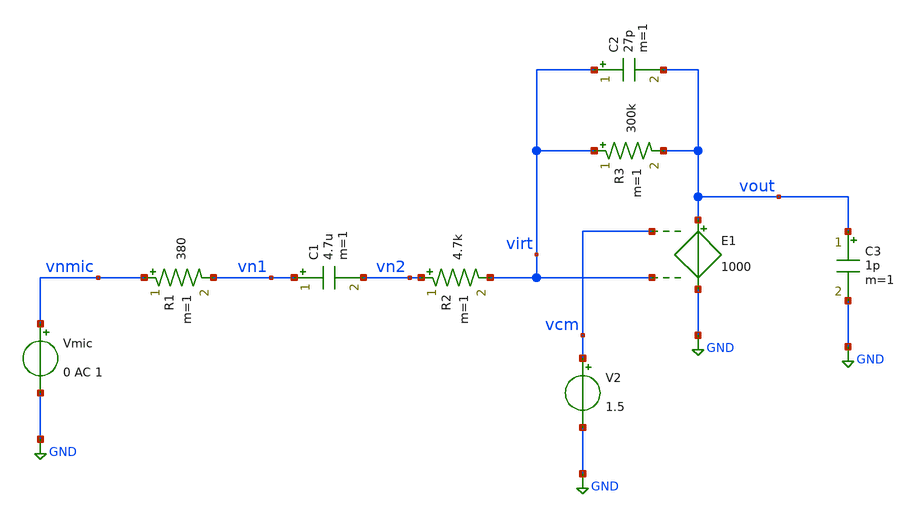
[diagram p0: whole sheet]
** sch_path: xschem/micTest.sch
**.subckt micTest
Vmic vnmic GND 0 AC 1
R1 vnmic vn1 380 m=1
C1 vn1 vn2 4.7u m=1
R2 vn2 virt 4.7k m=1
E1 vout GND vcm virt 1000
R3 virt vout 300k m=1
C2 virt vout 27p m=1
V2 vcm GND 1.5
C3 vout GND 1p m=1
**.ends
.GLOBAL GND
.end
